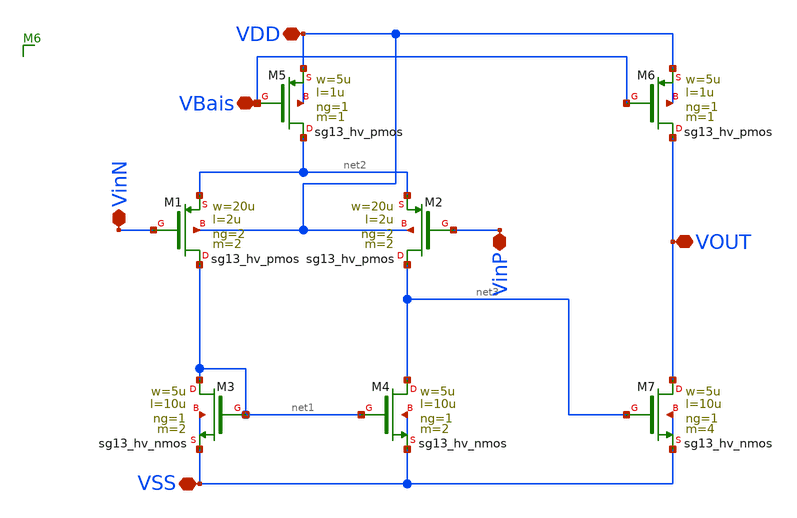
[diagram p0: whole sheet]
** sch_path: Design/Comp_2Stage/Comp_2Stage.sch
**.subckt Comp_2Stage VDD VBais VinP VinN VOUT VSS
*.iopin VDD
*.iopin VBais
*.iopin VinP
*.iopin VinN
*.iopin VOUT
*.iopin VSS
XM3 net1 net1 VSS VSS sg13_hv_nmos w=5u l=10u ng=1 m=2 mm_ok=1
XM1 net1 VinN net2 VDD sg13_hv_pmos w=20u l=2u ng=2 m=2 mm_ok=1
XM2 net3 VinP net2 VDD sg13_hv_pmos w=20u l=2u ng=2 m=2 mm_ok=1
XM4 net3 net1 VSS VSS sg13_hv_nmos w=5u l=10u ng=1 m=2 mm_ok=1
XM5 net2 VBais VDD VDD sg13_hv_pmos w=5u l=1u ng=1 m=1 mm_ok=1
XM6 VOUT VBais VDD VDD sg13_hv_pmos w=5u l=1u ng=1 m=1 mm_ok=1
XM7 VOUT net3 VSS VSS sg13_hv_nmos w=5u l=10u ng=1 m=4 mm_ok=1
**.ends
.end
